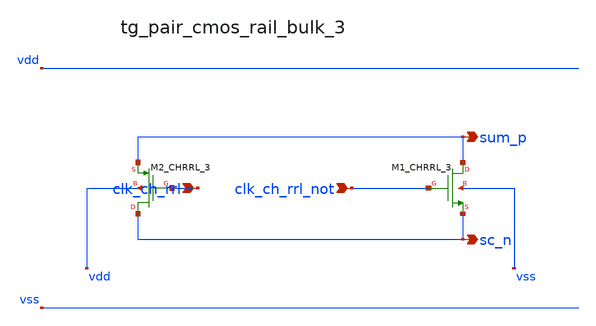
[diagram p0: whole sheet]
** sch_path: analog-db/raw/sup_003_rrl_sc_integrator/hier/blocks/tg_pair_cmos_rail_bulk_3.sch
**.subckt tg_pair_cmos_rail_bulk_3 clk_ch_rrl clk_ch_rrl_not sum_p sc_n
*.ipin clk_ch_rrl
*.ipin clk_ch_rrl_not
*.opin sum_p
*.opin sc_n
XM1_CHRRL_3 sum_p clk_ch_rrl_not sc_n vss sg13_lv_nmos w=x_dut_xm1_chrrl_3_w l=x_dut_xm1_chrrl_3_l
+ ng=1 m=x_dut_xm1_chrrl_3_m
XM2_CHRRL_3 sc_n clk_ch_rrl sum_p vdd sg13_lv_pmos w=x_dut_xm2_chrrl_3_w l=x_dut_xm2_chrrl_3_l ng=1
+ m=x_dut_xm2_chrrl_3_m
**.ends
.end
